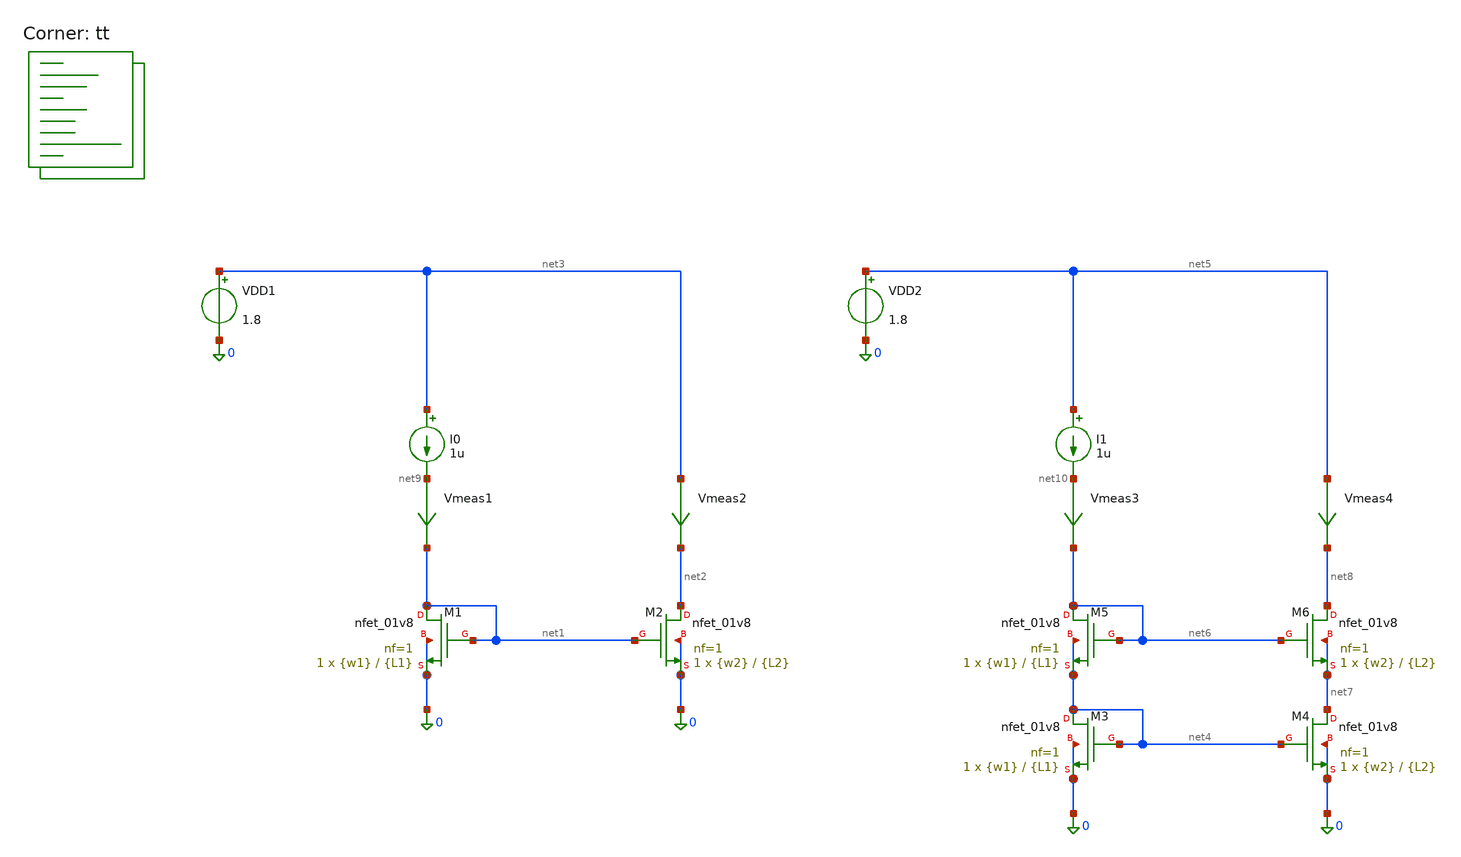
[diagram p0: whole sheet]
** sch_path: Training-3/cascode.sch
**.subckt cascode
XM1 net1 net1 0 0 sky130_fd_pr__nfet_01v8 L={L1} W={w1} nf=1 ad='int((nf+1)/2) * W/nf * 0.29' as='int((nf+2)/2) * W/nf * 0.29'
+ pd='2*int((nf+1)/2) * (W/nf + 0.29)' ps='2*int((nf+2)/2) * (W/nf + 0.29)' nrd='0.29 / W' nrs='0.29 / W'
+ sa=0 sb=0 sd=0 mult=1 m=1
XM2 net2 net1 0 0 sky130_fd_pr__nfet_01v8 L={L2} W={w2} nf=1 ad='int((nf+1)/2) * W/nf * 0.29' as='int((nf+2)/2) * W/nf * 0.29'
+ pd='2*int((nf+1)/2) * (W/nf + 0.29)' ps='2*int((nf+2)/2) * (W/nf + 0.29)' nrd='0.29 / W' nrs='0.29 / W'
+ sa=0 sb=0 sd=0 mult=1 m=1
Vmeas1 net9 net1 0
.save i(vmeas1)
Vmeas2 net3 net2 0
.save i(vmeas2)
VDD1 net3 0 1.8
I0 net3 net9 1u
XM3 net4 net4 0 0 sky130_fd_pr__nfet_01v8 L={L1} W={w1} nf=1 ad='int((nf+1)/2) * W/nf * 0.29' as='int((nf+2)/2) * W/nf * 0.29'
+ pd='2*int((nf+1)/2) * (W/nf + 0.29)' ps='2*int((nf+2)/2) * (W/nf + 0.29)' nrd='0.29 / W' nrs='0.29 / W'
+ sa=0 sb=0 sd=0 mult=1 m=1
XM4 net7 net4 0 0 sky130_fd_pr__nfet_01v8 L={L2} W={w2} nf=1 ad='int((nf+1)/2) * W/nf * 0.29' as='int((nf+2)/2) * W/nf * 0.29'
+ pd='2*int((nf+1)/2) * (W/nf + 0.29)' ps='2*int((nf+2)/2) * (W/nf + 0.29)' nrd='0.29 / W' nrs='0.29 / W'
+ sa=0 sb=0 sd=0 mult=1 m=1
Vmeas3 net10 net6 0
.save i(vmeas3)
Vmeas4 net5 net8 0
.save i(vmeas4)
VDD2 net5 0 1.8
I1 net5 net10 1u
XM5 net6 net6 net4 net4 sky130_fd_pr__nfet_01v8 L={L1} W={w1} nf=1 ad='int((nf+1)/2) * W/nf * 0.29' as='int((nf+2)/2) * W/nf * 0.29'
+ pd='2*int((nf+1)/2) * (W/nf + 0.29)' ps='2*int((nf+2)/2) * (W/nf + 0.29)' nrd='0.29 / W' nrs='0.29 / W'
+ sa=0 sb=0 sd=0 mult=1 m=1
XM6 net8 net6 net7 net7 sky130_fd_pr__nfet_01v8 L={L2} W={w2} nf=1 ad='int((nf+1)/2) * W/nf * 0.29' as='int((nf+2)/2) * W/nf * 0.29'
+ pd='2*int((nf+1)/2) * (W/nf + 0.29)' ps='2*int((nf+2)/2) * (W/nf + 0.29)' nrd='0.29 / W' nrs='0.29 / W'
+ sa=0 sb=0 sd=0 mult=1 m=1
**** begin user architecture code



.param L1 = 0.3
.param L2 = 0.3

.param w1 = 3
.param w2 = 3

.save
.control

*dc vdd1 0 1.8 0.01
*plot i(vmeas1) i(vmeas2) i(vmeas4)

tran 1n 100n
plot i(vmeas1) i(vmeas2) i(vmeas4)

op
let error1 = i(vmeas2)- i(vmeas1)
let error2 = i(vmeas4)- i(vmeas1)
print i(vmeas1) i(vmeas2) i(vmeas4)
print error1 error2

.endc




.lib $::SKYWATER_MODELS/sky130.lib.spice tt
**** end user architecture code
**.ends
.end
